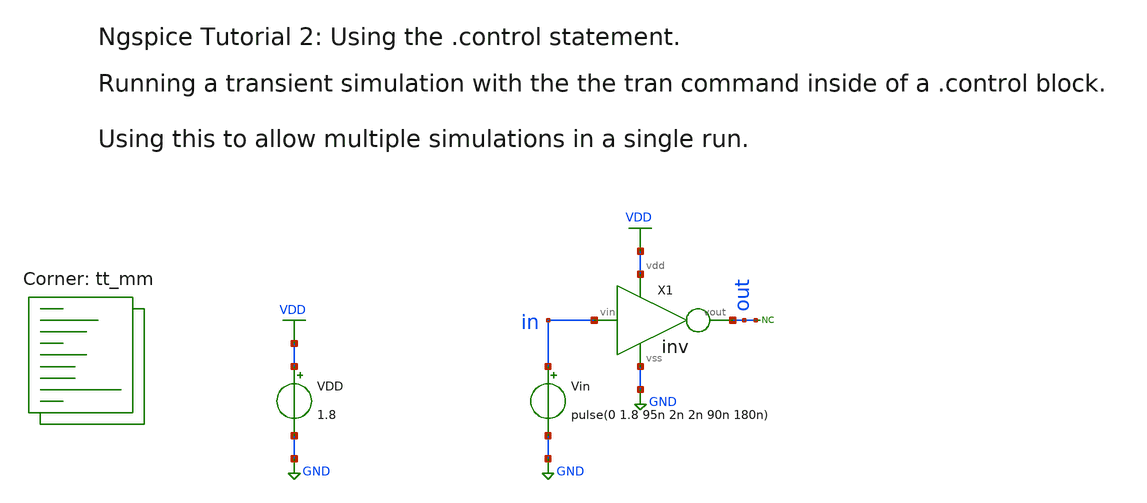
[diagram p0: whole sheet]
** sch_path: xsch/tut/ngspice_tut2_mc.sch
**.subckt ngspice_tut2_mc
Vin in GND pulse(0 1.8 95n 2n 2n 90n 180n)
VDD VDD GND 1.8
X1 in out VDD GND inv
* noconn out
**** begin user architecture code



* control language script

.control
set wr_vecnames
set wr_singlescale

let mc_runs = 10
let run = 1

dowhile run <= mc_runs

	tran 100p 500n						; simulation command 1
	set xbrushwidth=2						; set linewidth of the graph
	write $inputdir/ngspice_tut2_mc_tran_{$&run}.txt v(in) v(out)
	reset

	dc vin 0 1.8 0.01						; simulation command 2
	write $inputdir/ngspice_tut2_mc_dc_{$&run}.txt v(out)
	reset
	let run = run + 1;
end
plot dc1.v(out) dc2.v(out) dc3.v(out) dc4.v(out) dc5.v(out) dc6.v(out) dc7.v(out) dc8.v(out)
+ dc9.v(out) dc10.v(out)
.endc
.end



.lib $::SKYWATER_MODELS/sky130.lib.spice tt_mm
**** end user architecture code
**.ends
.GLOBAL VDD
.GLOBAL GND
.end
